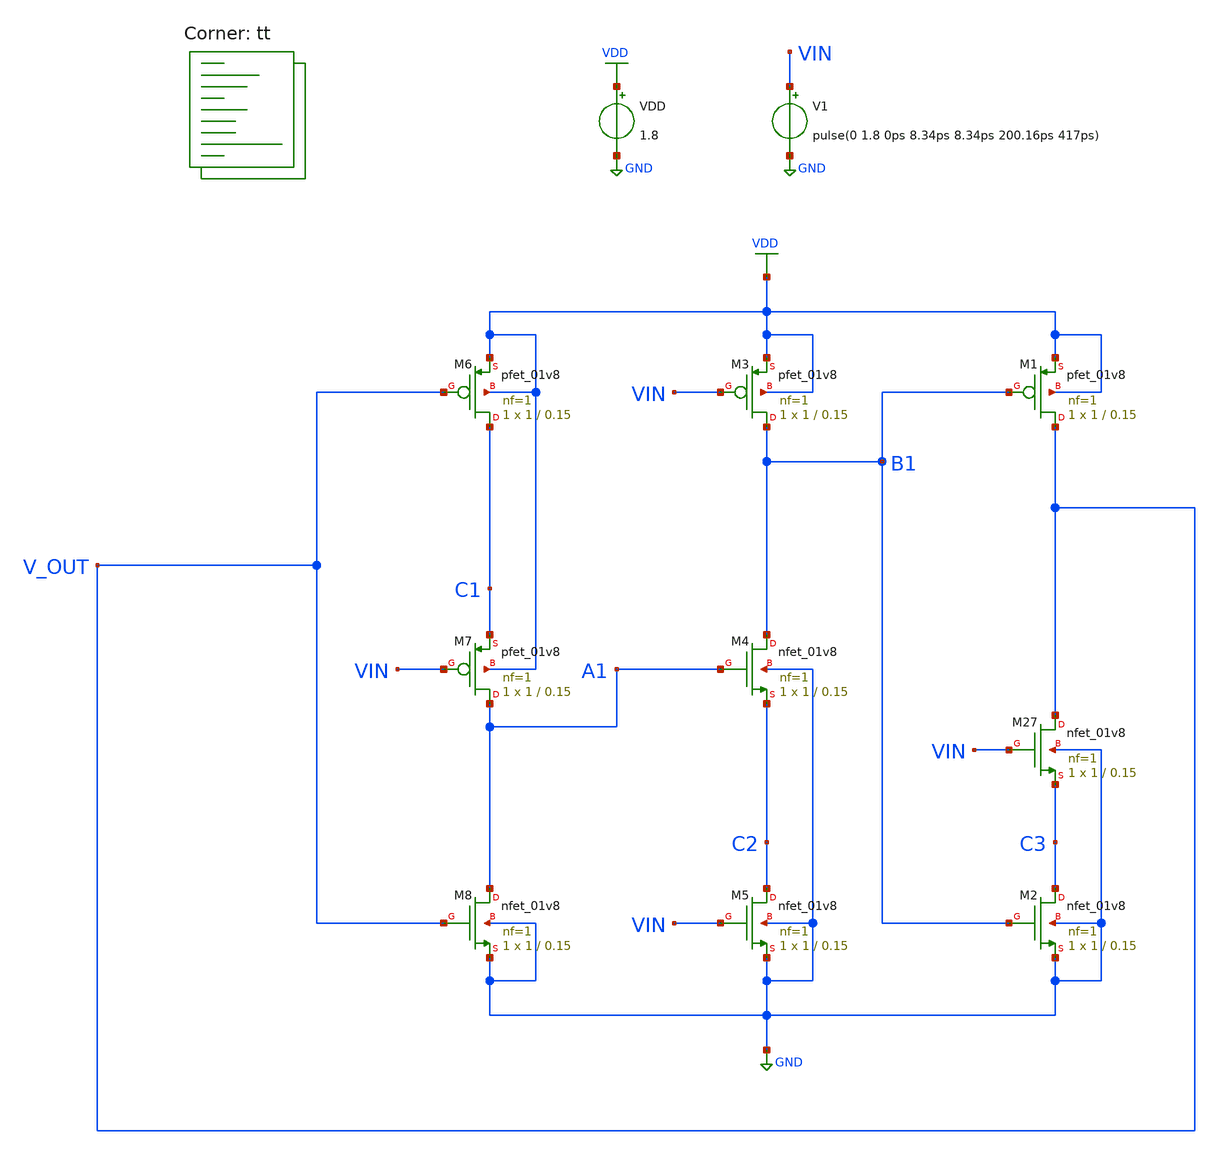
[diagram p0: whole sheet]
** sch_path: projects/pll/divider/xschem_ngspice/tb_TSPC_FF_divide3_2.sch
**.subckt tb_TSPC_FF_divide3_2
VDD VDD GND 1.8
XM1 V_OUT B1 VDD VDD sky130_fd_pr__pfet_01v8 L=0.15 W=1 nf=1 ad='int((nf+1)/2) * W/nf * 0.29' as='int((nf+2)/2) * W/nf * 0.29'
+ pd='2*int((nf+1)/2) * (W/nf + 0.29)' ps='2*int((nf+2)/2) * (W/nf + 0.29)' nrd='0.29 / W' nrs='0.29 / W'
+ sa=0 sb=0 sd=0 mult=1 m=1
XM4 B1 A1 C2 GND sky130_fd_pr__nfet_01v8 L=0.15 W=1 nf=1 ad='int((nf+1)/2) * W/nf * 0.29' as='int((nf+2)/2) * W/nf * 0.29'
+ pd='2*int((nf+1)/2) * (W/nf + 0.29)' ps='2*int((nf+2)/2) * (W/nf + 0.29)' nrd='0.29 / W' nrs='0.29 / W'
+ sa=0 sb=0 sd=0 mult=1 m=1
XM2 C3 B1 GND GND sky130_fd_pr__nfet_01v8 L=0.15 W=1 nf=1 ad='int((nf+1)/2) * W/nf * 0.29' as='int((nf+2)/2) * W/nf * 0.29'
+ pd='2*int((nf+1)/2) * (W/nf + 0.29)' ps='2*int((nf+2)/2) * (W/nf + 0.29)' nrd='0.29 / W' nrs='0.29 / W'
+ sa=0 sb=0 sd=0 mult=1 m=1
XM3 B1 VIN VDD VDD sky130_fd_pr__pfet_01v8 L=0.15 W=1 nf=1 ad='int((nf+1)/2) * W/nf * 0.29' as='int((nf+2)/2) * W/nf * 0.29'
+ pd='2*int((nf+1)/2) * (W/nf + 0.29)' ps='2*int((nf+2)/2) * (W/nf + 0.29)' nrd='0.29 / W' nrs='0.29 / W'
+ sa=0 sb=0 sd=0 mult=1 m=1
XM5 C2 VIN GND GND sky130_fd_pr__nfet_01v8 L=0.15 W=1 nf=1 ad='int((nf+1)/2) * W/nf * 0.29' as='int((nf+2)/2) * W/nf * 0.29'
+ pd='2*int((nf+1)/2) * (W/nf + 0.29)' ps='2*int((nf+2)/2) * (W/nf + 0.29)' nrd='0.29 / W' nrs='0.29 / W'
+ sa=0 sb=0 sd=0 mult=1 m=1
XM6 C1 V_OUT VDD VDD sky130_fd_pr__pfet_01v8 L=0.15 W=1 nf=1 ad='int((nf+1)/2) * W/nf * 0.29' as='int((nf+2)/2) * W/nf * 0.29'
+ pd='2*int((nf+1)/2) * (W/nf + 0.29)' ps='2*int((nf+2)/2) * (W/nf + 0.29)' nrd='0.29 / W' nrs='0.29 / W'
+ sa=0 sb=0 sd=0 mult=1 m=1
XM8 A1 V_OUT GND GND sky130_fd_pr__nfet_01v8 L=0.15 W=1 nf=1 ad='int((nf+1)/2) * W/nf * 0.29' as='int((nf+2)/2) * W/nf * 0.29'
+ pd='2*int((nf+1)/2) * (W/nf + 0.29)' ps='2*int((nf+2)/2) * (W/nf + 0.29)' nrd='0.29 / W' nrs='0.29 / W'
+ sa=0 sb=0 sd=0 mult=1 m=1
XM7 A1 VIN C1 VDD sky130_fd_pr__pfet_01v8 L=0.15 W=1 nf=1 ad='int((nf+1)/2) * W/nf * 0.29' as='int((nf+2)/2) * W/nf * 0.29'
+ pd='2*int((nf+1)/2) * (W/nf + 0.29)' ps='2*int((nf+2)/2) * (W/nf + 0.29)' nrd='0.29 / W' nrs='0.29 / W'
+ sa=0 sb=0 sd=0 mult=1 m=1
XM27 V_OUT VIN C3 GND sky130_fd_pr__nfet_01v8 L=0.15 W=1 nf=1 ad='int((nf+1)/2) * W/nf * 0.29' as='int((nf+2)/2) * W/nf * 0.29'
+ pd='2*int((nf+1)/2) * (W/nf + 0.29)' ps='2*int((nf+2)/2) * (W/nf + 0.29)' nrd='0.29 / W' nrs='0.29 / W'
+ sa=0 sb=0 sd=0 mult=1 m=1
V1 VIN GND pulse(0 1.8 0ps 8.34ps 8.34ps 200.16ps 417ps)
**** begin user architecture code



.include /foss/pdks/sky130A/libs.ref/sky130_fd_sc_hd/spice/sky130_fd_sc_hd.spice


.save @m.xm1.msky130_fd_pr__pfet_01v8[gm] @m.xm27.msky130_fd_pr__nfet_01v8[gm] @m.xm2.msky130_fd_pr__nfet_01v8[gm] @m.xm3.msky130_fd_pr__pfet_01v8[gm] @m.xm4.msky130_fd_pr__nfet_01v8[gm] @m.xm5.msky130_fd_pr__nfet_01v8[gm] @m.xm6.msky130_fd_pr__pfet_01v8[gm] @m.xm7.msky130_fd_pr__pfet_01v8[gm] @m.xm8.msky130_fd_pr__nfet_01v8[gm]

.option method=gear
.option wnflag=1
.option savecurrents


*.ic v(d)=0
.ic v(q1_b)=1.8
.ic v(q2_b)=1.8

.control

  save v(d1) v(d2) v(q1) v(q2) v(q1_b) v(q2_b) v(q3) v(q4) v(q3_b) v(q4_b) v(a1) v(a2) v(a3) v(a4)
+ v(b1) v(b2) v(b3) v(b4) v(c1) v(c2) v(c3) v(c4) v(c5) v(c6) v(c7) v(c8) v(ck) v(ck1) v(ck1_b)
  * save all
  * tran 0.1n 1u
  tran 0.5p 20n

  remzerovec
  write tb_TSPC_FF_divide2.raw
  * set appendwrite

.endc



.lib $::SKYWATER_MODELS/sky130.lib.spice tt
**** end user architecture code
**.ends
.GLOBAL GND
.GLOBAL VDD
.end
